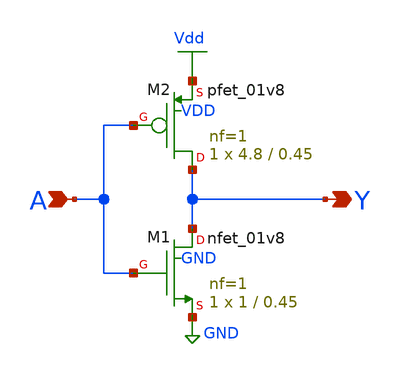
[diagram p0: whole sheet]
** sch_path: Circuiti/logic_gates_sch_sym/not.sch
**.subckt not A Y
*.ipin A
*.opin Y
XM1 Y A GND GND sky130_fd_pr__nfet_01v8 L=0.45 W=1 nf=1 ad='int((nf+1)/2) * W/nf * 0.29' as='int((nf+2)/2) * W/nf * 0.29'
+ pd='2*int((nf+1)/2) * (W/nf + 0.29)' ps='2*int((nf+2)/2) * (W/nf + 0.29)' nrd='0.29 / W' nrs='0.29 / W'
+ sa=0 sb=0 sd=0 mult=1 m=1
XM2 Y A Vdd VDD sky130_fd_pr__pfet_01v8 L=0.45 W=4.8 nf=1 ad='int((nf+1)/2) * W/nf * 0.29' as='int((nf+2)/2) * W/nf * 0.29'
+ pd='2*int((nf+1)/2) * (W/nf + 0.29)' ps='2*int((nf+2)/2) * (W/nf + 0.29)' nrd='0.29 / W' nrs='0.29 / W'
+ sa=0 sb=0 sd=0 mult=1 m=1
**.ends
.GLOBAL Vdd
.GLOBAL GND
.end
